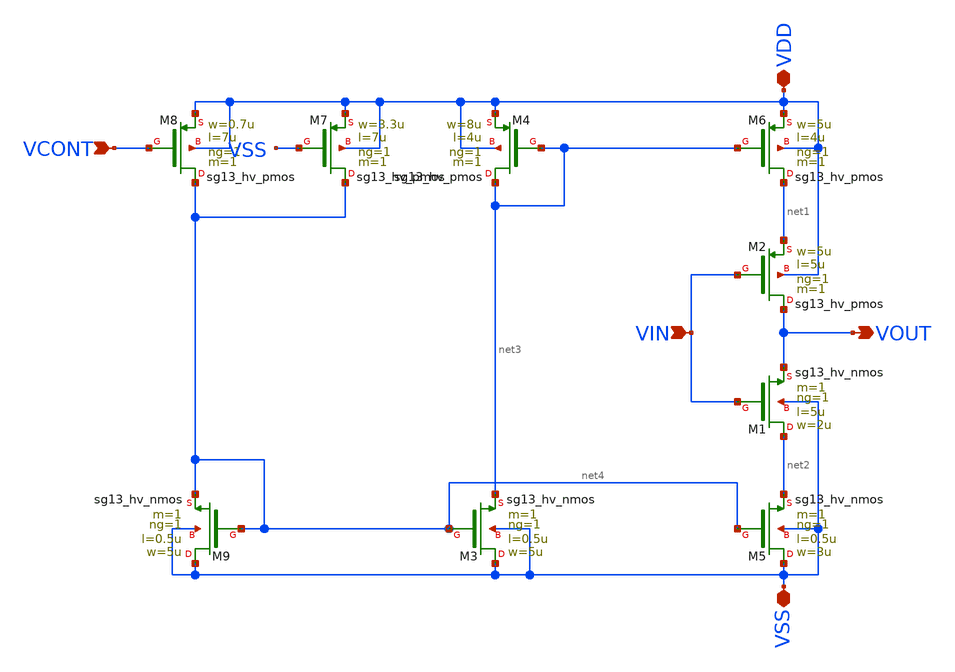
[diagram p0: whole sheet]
** sch_path: ChipUSM_AnalogTrack24/VCO/stage_vto2p1.sch
**.subckt stage_vto2p1 VIN VOUT VDD VSS VCONT
*.ipin VIN
*.opin VOUT
*.iopin VDD
*.iopin VSS
*.ipin VCONT
XM9 VSS net4 net4 VSS sg13_hv_nmos w=5u l=0.5u ng=1 m=1 mm_ok=1
XM3 VSS net4 net3 VSS sg13_hv_nmos w=5u l=0.5u ng=1 m=1 mm_ok=1
XM5 VSS net4 net2 VSS sg13_hv_nmos w=3u l=0.5u ng=1 m=1 mm_ok=1
XM8 net4 VCONT VDD VDD sg13_hv_pmos w=0.7u l=7u ng=1 m=1 mm_ok=1
XM4 net3 net3 VDD VDD sg13_hv_pmos w=8u l=4u ng=1 m=1 mm_ok=1
XM6 net1 net3 VDD VDD sg13_hv_pmos w=5u l=4u ng=1 m=1 mm_ok=1
XM2 VOUT VIN net1 VDD sg13_hv_pmos w=5u l=5u ng=1 m=1 mm_ok=1
XM1 net2 VIN VOUT VSS sg13_hv_nmos w=2u l=5u ng=1 m=1 mm_ok=1
XM7 net4 VSS VDD VDD sg13_hv_pmos w=3.3u l=7u ng=1 m=1 mm_ok=1
**.ends
.end
